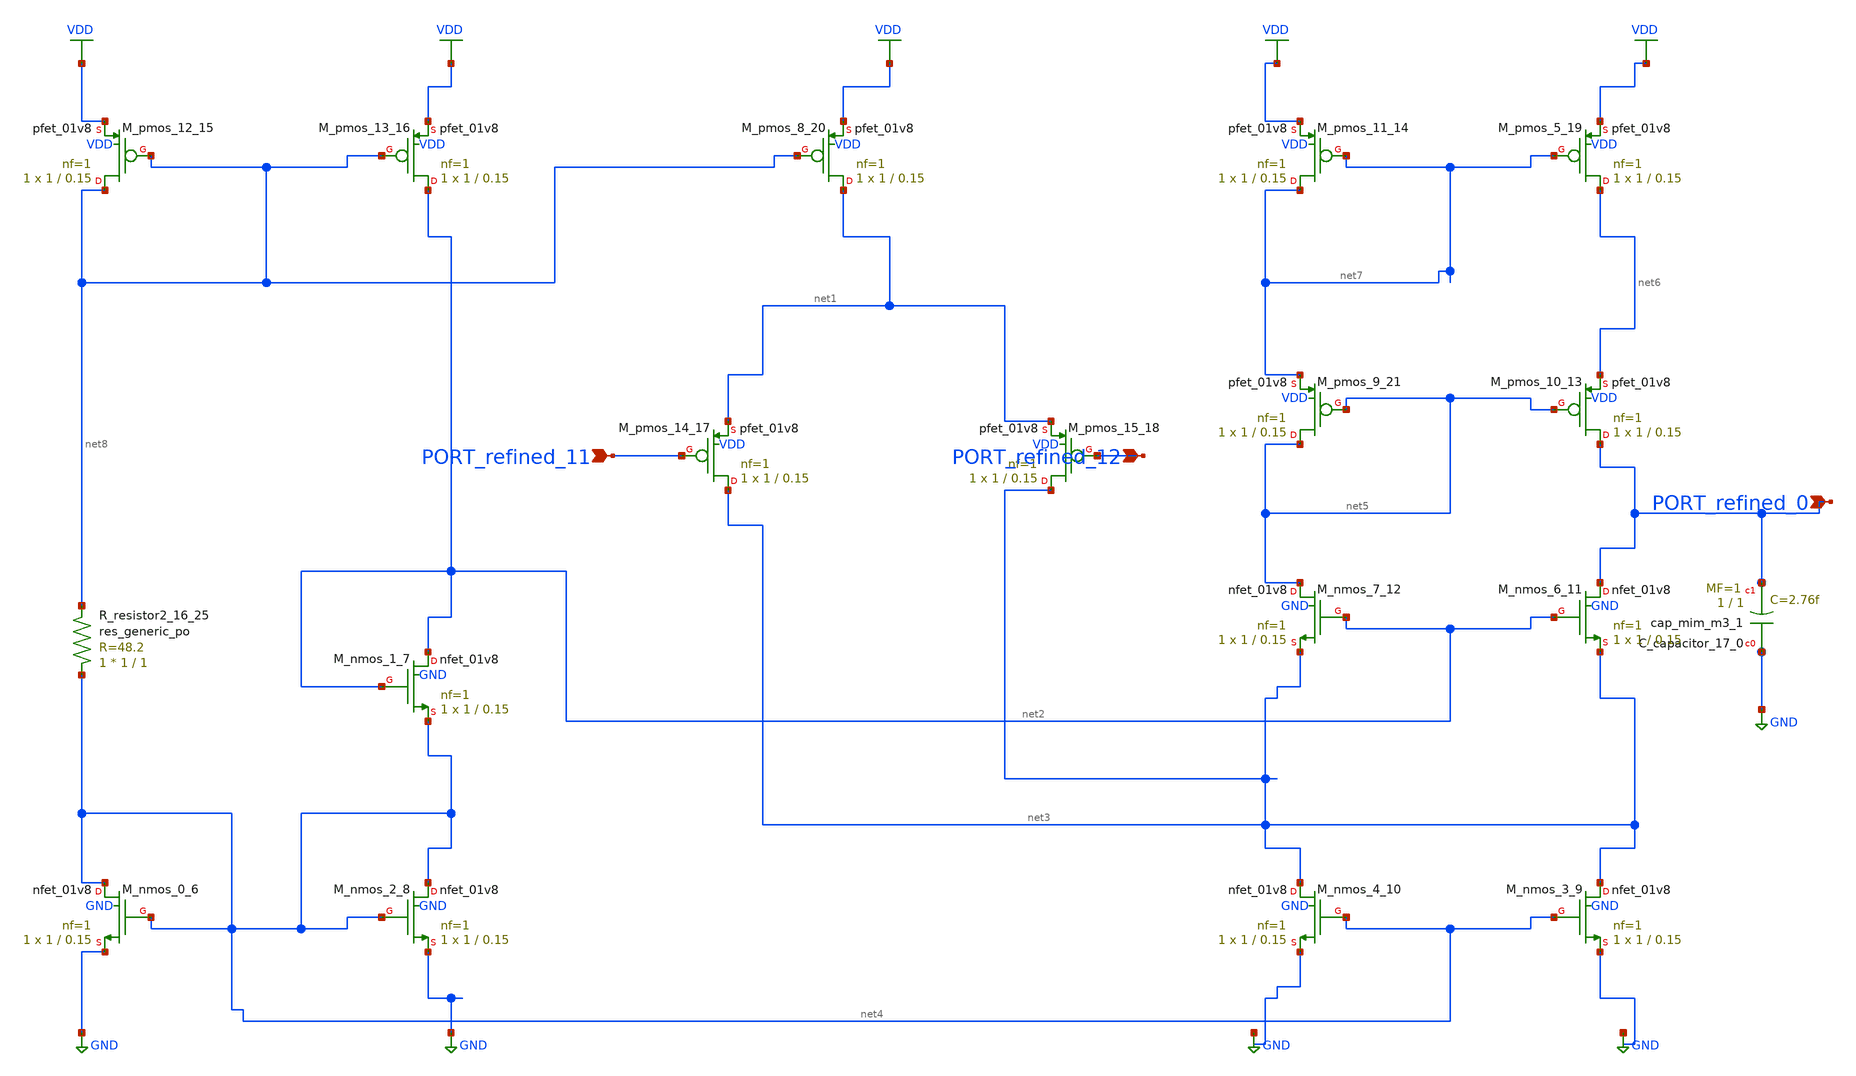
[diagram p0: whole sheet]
** sch_path: schematics/Image2Net/083.sch
**.subckt 083 PORT_refined_0 PORT_refined_12 PORT_refined_11
*.ipin PORT_refined_0
*.ipin PORT_refined_12
*.ipin PORT_refined_11
XC_capacitor_17_0 GND PORT_refined_0 sky130_fd_pr__cap_mim_m3_1 W=1 L=1 MF=1 m=1
XM_nmos_0_6 net4 net4 GND GND sky130_fd_pr__nfet_01v8 L=0.15 W=1 nf=1 ad='int((1 + 1)/2) * 1 / 1 * 0.29'
+ as='int((1 + 2)/2) * 1 / 1 * 0.29' pd='2*int((1 + 1)/2) * (1 / 1 + 0.29)' ps='2*int((1 + 2)/2) * (1 / 1 + 0.29)'
+ nrd='0.29 / 1 ' nrs='0.29 / 1 ' sa=0 sb=0 sd=0 mult=1 m=1
XM_nmos_1_7 net2 net2 net4 GND sky130_fd_pr__nfet_01v8 L=0.15 W=1 nf=1 ad='int((1 + 1)/2) * 1 / 1 * 0.29'
+ as='int((1 + 2)/2) * 1 / 1 * 0.29' pd='2*int((1 + 1)/2) * (1 / 1 + 0.29)' ps='2*int((1 + 2)/2) * (1 / 1 + 0.29)'
+ nrd='0.29 / 1 ' nrs='0.29 / 1 ' sa=0 sb=0 sd=0 mult=1 m=1
XM_nmos_2_8 net4 net4 GND GND sky130_fd_pr__nfet_01v8 L=0.15 W=1 nf=1 ad='int((1 + 1)/2) * 1 / 1 * 0.29'
+ as='int((1 + 2)/2) * 1 / 1 * 0.29' pd='2*int((1 + 1)/2) * (1 / 1 + 0.29)' ps='2*int((1 + 2)/2) * (1 / 1 + 0.29)'
+ nrd='0.29 / 1 ' nrs='0.29 / 1 ' sa=0 sb=0 sd=0 mult=1 m=1
XM_nmos_3_9 net3 net4 GND GND sky130_fd_pr__nfet_01v8 L=0.15 W=1 nf=1 ad='int((1 + 1)/2) * 1 / 1 * 0.29'
+ as='int((1 + 2)/2) * 1 / 1 * 0.29' pd='2*int((1 + 1)/2) * (1 / 1 + 0.29)' ps='2*int((1 + 2)/2) * (1 / 1 + 0.29)'
+ nrd='0.29 / 1 ' nrs='0.29 / 1 ' sa=0 sb=0 sd=0 mult=1 m=1
XM_nmos_4_10 net3 net4 GND GND sky130_fd_pr__nfet_01v8 L=0.15 W=1 nf=1 ad='int((1 + 1)/2) * 1 / 1 * 0.29'
+ as='int((1 + 2)/2) * 1 / 1 * 0.29' pd='2*int((1 + 1)/2) * (1 / 1 + 0.29)' ps='2*int((1 + 2)/2) * (1 / 1 + 0.29)'
+ nrd='0.29 / 1 ' nrs='0.29 / 1 ' sa=0 sb=0 sd=0 mult=1 m=1
XM_nmos_6_11 PORT_refined_0 net2 net3 GND sky130_fd_pr__nfet_01v8 L=0.15 W=1 nf=1 ad='int((1 + 1)/2) * 1 / 1 * 0.29'
+ as='int((1 + 2)/2) * 1 / 1 * 0.29' pd='2*int((1 + 1)/2) * (1 / 1 + 0.29)' ps='2*int((1 + 2)/2) * (1 / 1 + 0.29)'
+ nrd='0.29 / 1 ' nrs='0.29 / 1 ' sa=0 sb=0 sd=0 mult=1 m=1
XM_nmos_7_12 net5 net2 net3 GND sky130_fd_pr__nfet_01v8 L=0.15 W=1 nf=1 ad='int((1 + 1)/2) * 1 / 1 * 0.29'
+ as='int((1 + 2)/2) * 1 / 1 * 0.29' pd='2*int((1 + 1)/2) * (1 / 1 + 0.29)' ps='2*int((1 + 2)/2) * (1 / 1 + 0.29)'
+ nrd='0.29 / 1 ' nrs='0.29 / 1 ' sa=0 sb=0 sd=0 mult=1 m=1
XM_pmos_10_13 PORT_refined_0 net5 net6 VDD sky130_fd_pr__pfet_01v8 L=0.15 W=1 nf=1 ad='int((1 + 1)/2) * 1 / 1 * 0.29'
+ as='int((1 + 2)/2) * 1 / 1 * 0.29' pd='2*int((1 + 1)/2) * (1 / 1 + 0.29)' ps='2*int((1 + 2)/2) * (1 / 1 + 0.29)'
+ nrd='0.29 / 1 ' nrs='0.29 / 1 ' sa=0 sb=0 sd=0 mult=1 m=1
XM_pmos_11_14 net7 net7 VDD VDD sky130_fd_pr__pfet_01v8 L=0.15 W=1 nf=1 ad='int((1 + 1)/2) * 1 / 1 * 0.29'
+ as='int((1 + 2)/2) * 1 / 1 * 0.29' pd='2*int((1 + 1)/2) * (1 / 1 + 0.29)' ps='2*int((1 + 2)/2) * (1 / 1 + 0.29)'
+ nrd='0.29 / 1 ' nrs='0.29 / 1 ' sa=0 sb=0 sd=0 mult=1 m=1
XM_pmos_12_15 net8 net8 VDD VDD sky130_fd_pr__pfet_01v8 L=0.15 W=1 nf=1 ad='int((1 + 1)/2) * 1 / 1 * 0.29'
+ as='int((1 + 2)/2) * 1 / 1 * 0.29' pd='2*int((1 + 1)/2) * (1 / 1 + 0.29)' ps='2*int((1 + 2)/2) * (1 / 1 + 0.29)'
+ nrd='0.29 / 1 ' nrs='0.29 / 1 ' sa=0 sb=0 sd=0 mult=1 m=1
XM_pmos_13_16 net2 net8 VDD VDD sky130_fd_pr__pfet_01v8 L=0.15 W=1 nf=1 ad='int((1 + 1)/2) * 1 / 1 * 0.29'
+ as='int((1 + 2)/2) * 1 / 1 * 0.29' pd='2*int((1 + 1)/2) * (1 / 1 + 0.29)' ps='2*int((1 + 2)/2) * (1 / 1 + 0.29)'
+ nrd='0.29 / 1 ' nrs='0.29 / 1 ' sa=0 sb=0 sd=0 mult=1 m=1
XM_pmos_14_17 net3 PORT_refined_11 net1 VDD sky130_fd_pr__pfet_01v8 L=0.15 W=1 nf=1 ad='int((1 + 1)/2) * 1 / 1 * 0.29'
+ as='int((1 + 2)/2) * 1 / 1 * 0.29' pd='2*int((1 + 1)/2) * (1 / 1 + 0.29)' ps='2*int((1 + 2)/2) * (1 / 1 + 0.29)'
+ nrd='0.29 / 1 ' nrs='0.29 / 1 ' sa=0 sb=0 sd=0 mult=1 m=1
XM_pmos_15_18 net3 PORT_refined_12 net1 VDD sky130_fd_pr__pfet_01v8 L=0.15 W=1 nf=1 ad='int((1 + 1)/2) * 1 / 1 * 0.29'
+ as='int((1 + 2)/2) * 1 / 1 * 0.29' pd='2*int((1 + 1)/2) * (1 / 1 + 0.29)' ps='2*int((1 + 2)/2) * (1 / 1 + 0.29)'
+ nrd='0.29 / 1 ' nrs='0.29 / 1 ' sa=0 sb=0 sd=0 mult=1 m=1
XM_pmos_5_19 net6 net7 VDD VDD sky130_fd_pr__pfet_01v8 L=0.15 W=1 nf=1 ad='int((1 + 1)/2) * 1 / 1 * 0.29'
+ as='int((1 + 2)/2) * 1 / 1 * 0.29' pd='2*int((1 + 1)/2) * (1 / 1 + 0.29)' ps='2*int((1 + 2)/2) * (1 / 1 + 0.29)'
+ nrd='0.29 / 1 ' nrs='0.29 / 1 ' sa=0 sb=0 sd=0 mult=1 m=1
XM_pmos_8_20 net1 net8 VDD VDD sky130_fd_pr__pfet_01v8 L=0.15 W=1 nf=1 ad='int((1 + 1)/2) * 1 / 1 * 0.29'
+ as='int((1 + 2)/2) * 1 / 1 * 0.29' pd='2*int((1 + 1)/2) * (1 / 1 + 0.29)' ps='2*int((1 + 2)/2) * (1 / 1 + 0.29)'
+ nrd='0.29 / 1 ' nrs='0.29 / 1 ' sa=0 sb=0 sd=0 mult=1 m=1
XM_pmos_9_21 net5 net5 net7 VDD sky130_fd_pr__pfet_01v8 L=0.15 W=1 nf=1 ad='int((1 + 1)/2) * 1 / 1 * 0.29'
+ as='int((1 + 2)/2) * 1 / 1 * 0.29' pd='2*int((1 + 1)/2) * (1 / 1 + 0.29)' ps='2*int((1 + 2)/2) * (1 / 1 + 0.29)'
+ nrd='0.29 / 1 ' nrs='0.29 / 1 ' sa=0 sb=0 sd=0 mult=1 m=1
XR_resistor2_16_25 net4 net8 sky130_fd_pr__res_generic_po W=1 L=1 m=1
**.ends
.GLOBAL GND
.GLOBAL VDD
.end
